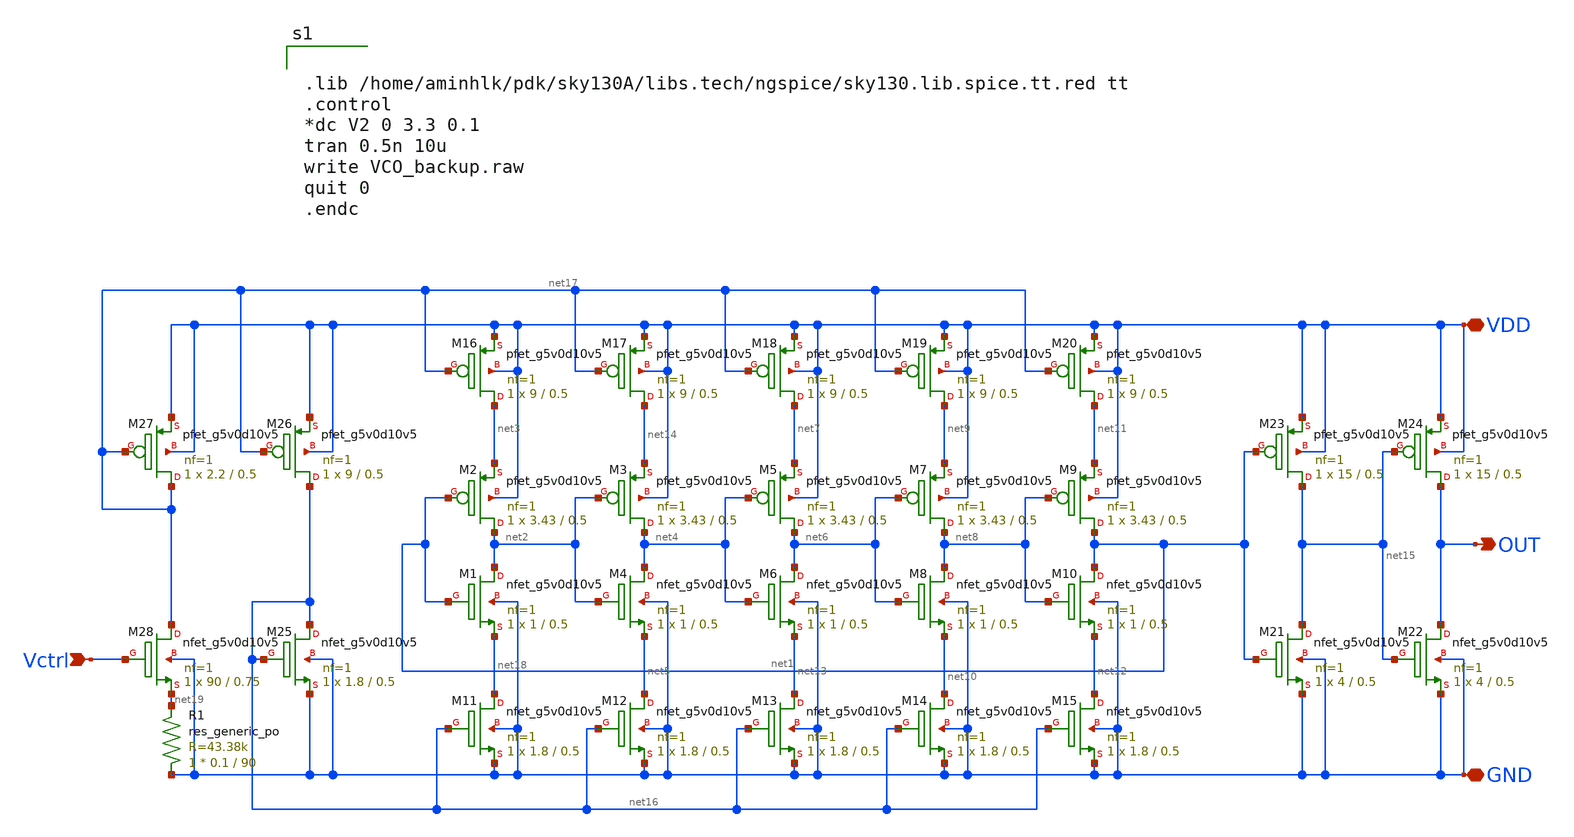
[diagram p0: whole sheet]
** sch_path: VCO/VCO_schematic.sch
**.subckt VCO_schematic Vctrl OUT VDD GND
*.ipin Vctrl
*.opin OUT
*.iopin VDD
*.iopin GND
XM2 net2 net1 net3 VDD sky130_fd_pr__pfet_g5v0d10v5 L=0.5 W=3.43 nf=1 ad='int((nf+1)/2) * W/nf * 0.29'
+ as='int((nf+2)/2) * W/nf * 0.29' pd='2*int((nf+1)/2) * (W/nf + 0.29)' ps='2*int((nf+2)/2) * (W/nf + 0.29)'
+ nrd='0.29 / W' nrs='0.29 / W' sa=0 sb=0 sd=0 mult=1 m=1
XM1 net2 net1 net18 GND sky130_fd_pr__nfet_g5v0d10v5 L=0.5 W=1 nf=1 ad='int((nf+1)/2) * W/nf * 0.29'
+ as='int((nf+2)/2) * W/nf * 0.29' pd='2*int((nf+1)/2) * (W/nf + 0.29)' ps='2*int((nf+2)/2) * (W/nf + 0.29)'
+ nrd='0.29 / W' nrs='0.29 / W' sa=0 sb=0 sd=0 mult=1 m=1
XM3 net4 net2 net14 VDD sky130_fd_pr__pfet_g5v0d10v5 L=0.5 W=3.43 nf=1 ad='int((nf+1)/2) * W/nf * 0.29'
+ as='int((nf+2)/2) * W/nf * 0.29' pd='2*int((nf+1)/2) * (W/nf + 0.29)' ps='2*int((nf+2)/2) * (W/nf + 0.29)'
+ nrd='0.29 / W' nrs='0.29 / W' sa=0 sb=0 sd=0 mult=1 m=1
XM4 net4 net2 net5 GND sky130_fd_pr__nfet_g5v0d10v5 L=0.5 W=1 nf=1 ad='int((nf+1)/2) * W/nf * 0.29' as='int((nf+2)/2) * W/nf * 0.29'
+ pd='2*int((nf+1)/2) * (W/nf + 0.29)' ps='2*int((nf+2)/2) * (W/nf + 0.29)' nrd='0.29 / W' nrs='0.29 / W'
+ sa=0 sb=0 sd=0 mult=1 m=1
XM5 net6 net4 net7 VDD sky130_fd_pr__pfet_g5v0d10v5 L=0.5 W=3.43 nf=1 ad='int((nf+1)/2) * W/nf * 0.29'
+ as='int((nf+2)/2) * W/nf * 0.29' pd='2*int((nf+1)/2) * (W/nf + 0.29)' ps='2*int((nf+2)/2) * (W/nf + 0.29)'
+ nrd='0.29 / W' nrs='0.29 / W' sa=0 sb=0 sd=0 mult=1 m=1
XM6 net6 net4 net13 GND sky130_fd_pr__nfet_g5v0d10v5 L=0.5 W=1 nf=1 ad='int((nf+1)/2) * W/nf * 0.29'
+ as='int((nf+2)/2) * W/nf * 0.29' pd='2*int((nf+1)/2) * (W/nf + 0.29)' ps='2*int((nf+2)/2) * (W/nf + 0.29)'
+ nrd='0.29 / W' nrs='0.29 / W' sa=0 sb=0 sd=0 mult=1 m=1
XM7 net8 net6 net9 VDD sky130_fd_pr__pfet_g5v0d10v5 L=0.5 W=3.43 nf=1 ad='int((nf+1)/2) * W/nf * 0.29'
+ as='int((nf+2)/2) * W/nf * 0.29' pd='2*int((nf+1)/2) * (W/nf + 0.29)' ps='2*int((nf+2)/2) * (W/nf + 0.29)'
+ nrd='0.29 / W' nrs='0.29 / W' sa=0 sb=0 sd=0 mult=1 m=1
XM8 net8 net6 net10 GND sky130_fd_pr__nfet_g5v0d10v5 L=0.5 W=1 nf=1 ad='int((nf+1)/2) * W/nf * 0.29'
+ as='int((nf+2)/2) * W/nf * 0.29' pd='2*int((nf+1)/2) * (W/nf + 0.29)' ps='2*int((nf+2)/2) * (W/nf + 0.29)'
+ nrd='0.29 / W' nrs='0.29 / W' sa=0 sb=0 sd=0 mult=1 m=1
XM9 net1 net8 net11 VDD sky130_fd_pr__pfet_g5v0d10v5 L=0.5 W=3.43 nf=1 ad='int((nf+1)/2) * W/nf * 0.29'
+ as='int((nf+2)/2) * W/nf * 0.29' pd='2*int((nf+1)/2) * (W/nf + 0.29)' ps='2*int((nf+2)/2) * (W/nf + 0.29)'
+ nrd='0.29 / W' nrs='0.29 / W' sa=0 sb=0 sd=0 mult=1 m=1
XM10 net1 net8 net12 GND sky130_fd_pr__nfet_g5v0d10v5 L=0.5 W=1 nf=1 ad='int((nf+1)/2) * W/nf * 0.29'
+ as='int((nf+2)/2) * W/nf * 0.29' pd='2*int((nf+1)/2) * (W/nf + 0.29)' ps='2*int((nf+2)/2) * (W/nf + 0.29)'
+ nrd='0.29 / W' nrs='0.29 / W' sa=0 sb=0 sd=0 mult=1 m=1
XM11 net18 net16 GND GND sky130_fd_pr__nfet_g5v0d10v5 L=0.5 W=1.8 nf=1 ad='int((nf+1)/2) * W/nf * 0.29'
+ as='int((nf+2)/2) * W/nf * 0.29' pd='2*int((nf+1)/2) * (W/nf + 0.29)' ps='2*int((nf+2)/2) * (W/nf + 0.29)'
+ nrd='0.29 / W' nrs='0.29 / W' sa=0 sb=0 sd=0 mult=1 m=1
XM12 net5 net16 GND GND sky130_fd_pr__nfet_g5v0d10v5 L=0.5 W=1.8 nf=1 ad='int((nf+1)/2) * W/nf * 0.29'
+ as='int((nf+2)/2) * W/nf * 0.29' pd='2*int((nf+1)/2) * (W/nf + 0.29)' ps='2*int((nf+2)/2) * (W/nf + 0.29)'
+ nrd='0.29 / W' nrs='0.29 / W' sa=0 sb=0 sd=0 mult=1 m=1
XM13 net13 net16 GND GND sky130_fd_pr__nfet_g5v0d10v5 L=0.5 W=1.8 nf=1 ad='int((nf+1)/2) * W/nf * 0.29'
+ as='int((nf+2)/2) * W/nf * 0.29' pd='2*int((nf+1)/2) * (W/nf + 0.29)' ps='2*int((nf+2)/2) * (W/nf + 0.29)'
+ nrd='0.29 / W' nrs='0.29 / W' sa=0 sb=0 sd=0 mult=1 m=1
XM14 net10 net16 GND GND sky130_fd_pr__nfet_g5v0d10v5 L=0.5 W=1.8 nf=1 ad='int((nf+1)/2) * W/nf * 0.29'
+ as='int((nf+2)/2) * W/nf * 0.29' pd='2*int((nf+1)/2) * (W/nf + 0.29)' ps='2*int((nf+2)/2) * (W/nf + 0.29)'
+ nrd='0.29 / W' nrs='0.29 / W' sa=0 sb=0 sd=0 mult=1 m=1
XM15 net12 net16 GND GND sky130_fd_pr__nfet_g5v0d10v5 L=0.5 W=1.8 nf=1 ad='int((nf+1)/2) * W/nf * 0.29'
+ as='int((nf+2)/2) * W/nf * 0.29' pd='2*int((nf+1)/2) * (W/nf + 0.29)' ps='2*int((nf+2)/2) * (W/nf + 0.29)'
+ nrd='0.29 / W' nrs='0.29 / W' sa=0 sb=0 sd=0 mult=1 m=1
XM16 net3 net17 VDD VDD sky130_fd_pr__pfet_g5v0d10v5 L=0.5 W=9 nf=1 ad='int((nf+1)/2) * W/nf * 0.29'
+ as='int((nf+2)/2) * W/nf * 0.29' pd='2*int((nf+1)/2) * (W/nf + 0.29)' ps='2*int((nf+2)/2) * (W/nf + 0.29)'
+ nrd='0.29 / W' nrs='0.29 / W' sa=0 sb=0 sd=0 mult=1 m=1
XM17 net14 net17 VDD VDD sky130_fd_pr__pfet_g5v0d10v5 L=0.5 W=9 nf=1 ad='int((nf+1)/2) * W/nf * 0.29'
+ as='int((nf+2)/2) * W/nf * 0.29' pd='2*int((nf+1)/2) * (W/nf + 0.29)' ps='2*int((nf+2)/2) * (W/nf + 0.29)'
+ nrd='0.29 / W' nrs='0.29 / W' sa=0 sb=0 sd=0 mult=1 m=1
XM18 net7 net17 VDD VDD sky130_fd_pr__pfet_g5v0d10v5 L=0.5 W=9 nf=1 ad='int((nf+1)/2) * W/nf * 0.29'
+ as='int((nf+2)/2) * W/nf * 0.29' pd='2*int((nf+1)/2) * (W/nf + 0.29)' ps='2*int((nf+2)/2) * (W/nf + 0.29)'
+ nrd='0.29 / W' nrs='0.29 / W' sa=0 sb=0 sd=0 mult=1 m=1
XM19 net9 net17 VDD VDD sky130_fd_pr__pfet_g5v0d10v5 L=0.5 W=9 nf=1 ad='int((nf+1)/2) * W/nf * 0.29'
+ as='int((nf+2)/2) * W/nf * 0.29' pd='2*int((nf+1)/2) * (W/nf + 0.29)' ps='2*int((nf+2)/2) * (W/nf + 0.29)'
+ nrd='0.29 / W' nrs='0.29 / W' sa=0 sb=0 sd=0 mult=1 m=1
XM20 net11 net17 VDD VDD sky130_fd_pr__pfet_g5v0d10v5 L=0.5 W=9 nf=1 ad='int((nf+1)/2) * W/nf * 0.29'
+ as='int((nf+2)/2) * W/nf * 0.29' pd='2*int((nf+1)/2) * (W/nf + 0.29)' ps='2*int((nf+2)/2) * (W/nf + 0.29)'
+ nrd='0.29 / W' nrs='0.29 / W' sa=0 sb=0 sd=0 mult=1 m=1
XM21 net15 net1 GND GND sky130_fd_pr__nfet_g5v0d10v5 L=0.5 W=4 nf=1 ad='int((nf+1)/2) * W/nf * 0.29'
+ as='int((nf+2)/2) * W/nf * 0.29' pd='2*int((nf+1)/2) * (W/nf + 0.29)' ps='2*int((nf+2)/2) * (W/nf + 0.29)'
+ nrd='0.29 / W' nrs='0.29 / W' sa=0 sb=0 sd=0 mult=1 m=1
XM22 OUT net15 GND GND sky130_fd_pr__nfet_g5v0d10v5 L=0.5 W=4 nf=1 ad='int((nf+1)/2) * W/nf * 0.29' as='int((nf+2)/2) * W/nf * 0.29'
+ pd='2*int((nf+1)/2) * (W/nf + 0.29)' ps='2*int((nf+2)/2) * (W/nf + 0.29)' nrd='0.29 / W' nrs='0.29 / W'
+ sa=0 sb=0 sd=0 mult=1 m=1
XM23 net15 net1 VDD VDD sky130_fd_pr__pfet_g5v0d10v5 L=0.5 W=15 nf=1 ad='int((nf+1)/2) * W/nf * 0.29'
+ as='int((nf+2)/2) * W/nf * 0.29' pd='2*int((nf+1)/2) * (W/nf + 0.29)' ps='2*int((nf+2)/2) * (W/nf + 0.29)'
+ nrd='0.29 / W' nrs='0.29 / W' sa=0 sb=0 sd=0 mult=1 m=1
XM24 OUT net15 VDD VDD sky130_fd_pr__pfet_g5v0d10v5 L=0.5 W=15 nf=1 ad='int((nf+1)/2) * W/nf * 0.29'
+ as='int((nf+2)/2) * W/nf * 0.29' pd='2*int((nf+1)/2) * (W/nf + 0.29)' ps='2*int((nf+2)/2) * (W/nf + 0.29)'
+ nrd='0.29 / W' nrs='0.29 / W' sa=0 sb=0 sd=0 mult=1 m=1
XM25 net16 net16 GND GND sky130_fd_pr__nfet_g5v0d10v5 L=0.5 W=1.8 nf=1 ad='int((nf+1)/2) * W/nf * 0.29'
+ as='int((nf+2)/2) * W/nf * 0.29' pd='2*int((nf+1)/2) * (W/nf + 0.29)' ps='2*int((nf+2)/2) * (W/nf + 0.29)'
+ nrd='0.29 / W' nrs='0.29 / W' sa=0 sb=0 sd=0 mult=1 m=1
XM26 net16 net17 VDD VDD sky130_fd_pr__pfet_g5v0d10v5 L=0.5 W=9 nf=1 ad='int((nf+1)/2) * W/nf * 0.29'
+ as='int((nf+2)/2) * W/nf * 0.29' pd='2*int((nf+1)/2) * (W/nf + 0.29)' ps='2*int((nf+2)/2) * (W/nf + 0.29)'
+ nrd='0.29 / W' nrs='0.29 / W' sa=0 sb=0 sd=0 mult=1 m=1
XM27 net17 net17 VDD VDD sky130_fd_pr__pfet_g5v0d10v5 L=0.5 W=2.2 nf=1 ad='int((nf+1)/2) * W/nf * 0.29'
+ as='int((nf+2)/2) * W/nf * 0.29' pd='2*int((nf+1)/2) * (W/nf + 0.29)' ps='2*int((nf+2)/2) * (W/nf + 0.29)'
+ nrd='0.29 / W' nrs='0.29 / W' sa=0 sb=0 sd=0 mult=1 m=1
XM28 net17 Vctrl net19 GND sky130_fd_pr__nfet_g5v0d10v5 L=0.75 W=90 nf=1 ad='int((nf+1)/2) * W/nf * 0.29'
+ as='int((nf+2)/2) * W/nf * 0.29' pd='2*int((nf+1)/2) * (W/nf + 0.29)' ps='2*int((nf+2)/2) * (W/nf + 0.29)'
+ nrd='0.29 / W' nrs='0.29 / W' sa=0 sb=0 sd=0 mult=1 m=1
XR1 GND net19 sky130_fd_pr__res_generic_po W=0.1 L=90 m=1
**** begin user architecture code


.lib /home/aminhlk/pdk/sky130A/libs.tech/ngspice/sky130.lib.spice.tt.red tt
.control
*dc V2 0 3.3 0.1
tran 0.5n 10u
write VCO_backup.raw
quit 0
.endc


**** end user architecture code
**.ends
.end
